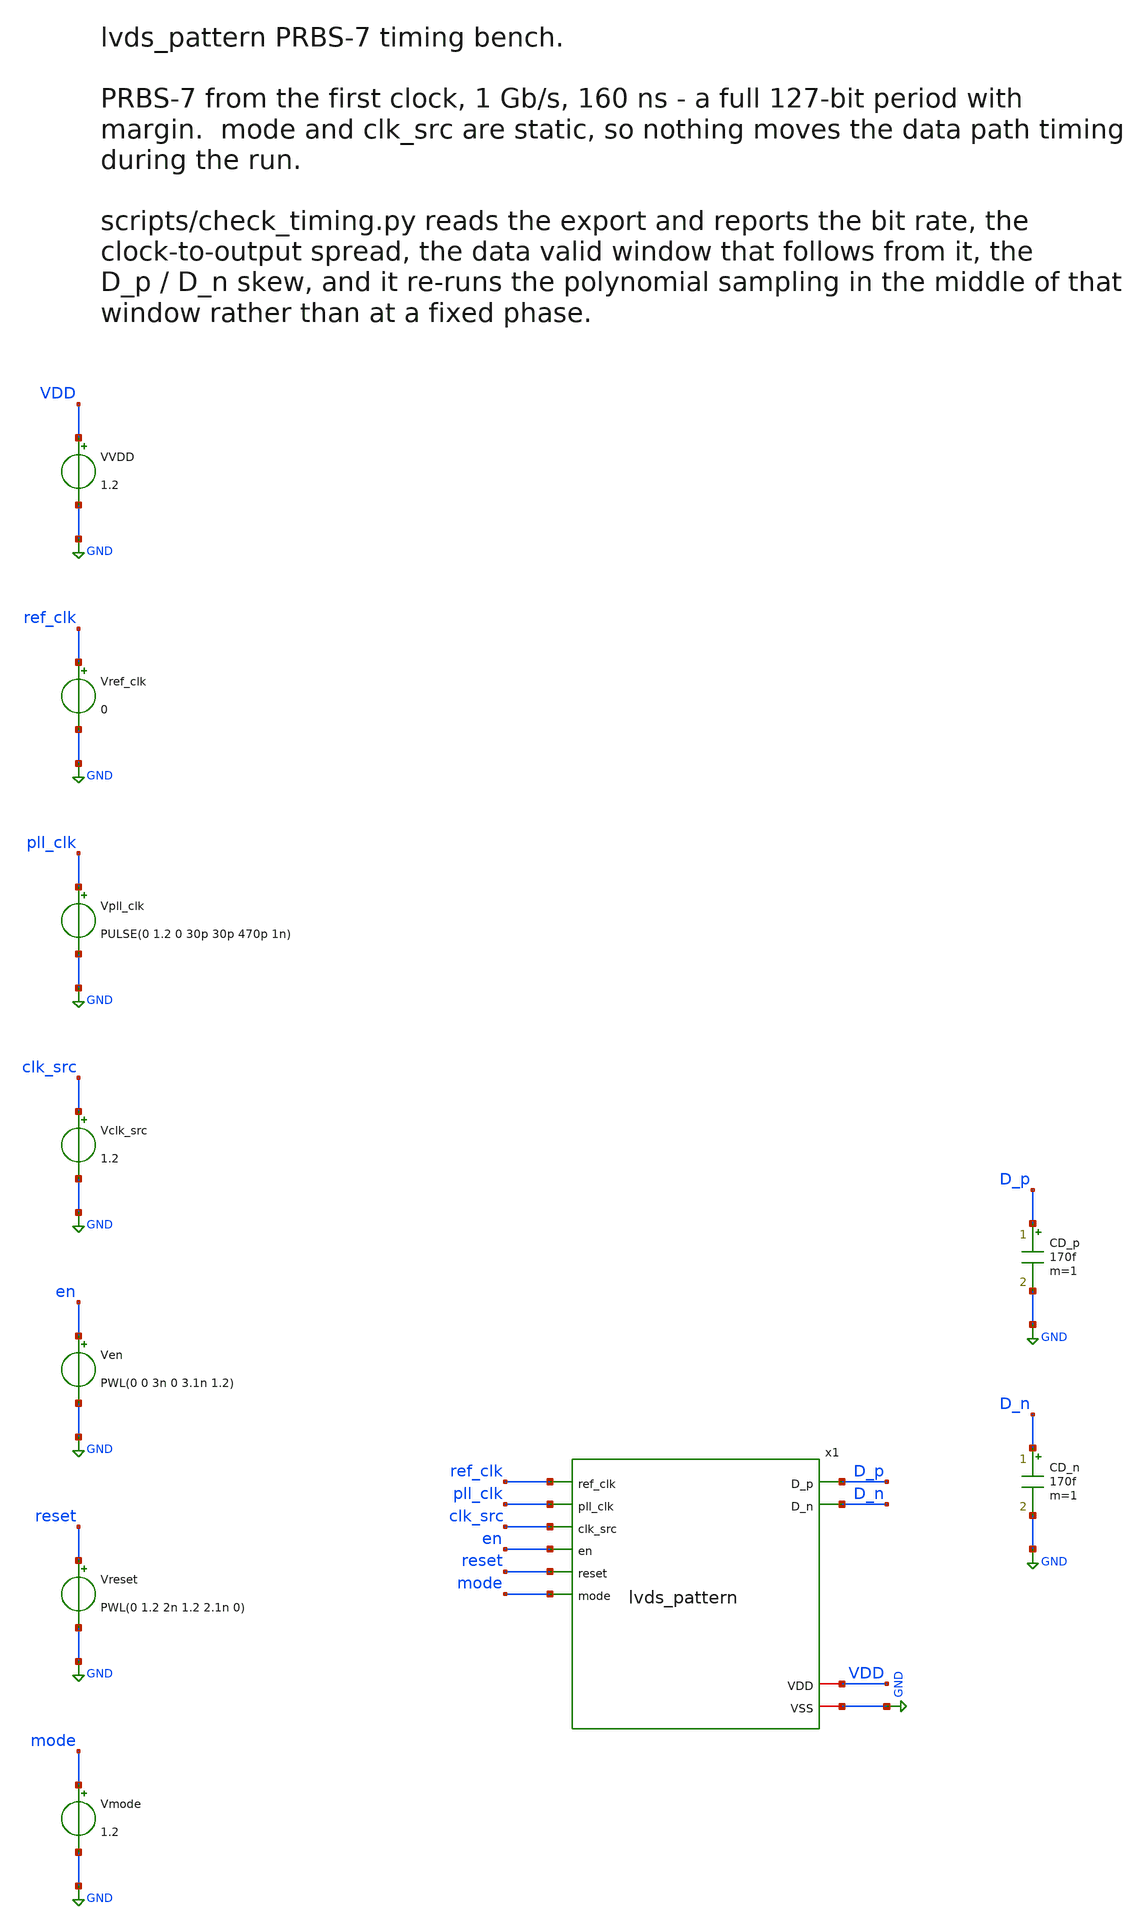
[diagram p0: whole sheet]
** sch_path: macros/lvds_pattern/testbenches/xschem/lvds_pattern_tb_prbs.sch
**.subckt lvds_pattern_tb_prbs
VVDD VDD GND 1.2
Vref_clk ref_clk GND 0
Vpll_clk pll_clk GND PULSE(0 1.2 0 30p 30p 470p 1n)
Vclk_src clk_src GND 1.2
Ven en GND PWL(0 0 3n 0 3.1n 1.2)
Vreset reset GND PWL(0 1.2 2n 1.2 2.1n 0)
Vmode mode GND 1.2
x1 ref_clk pll_clk clk_src en reset mode D_p D_n VDD GND lvds_pattern
CD_p D_p GND 170f m=1
CD_n D_n GND 170f m=1
**** begin user architecture code


.include /foss/pdks/ihp-sg13cmos5l/libs.ref/sg13cmos5l_stdcell/spice/sg13cmos5l_stdcell.spice
.lib cornerMOSlv.lib mos_tt
.temp 27
.options savecurrents klu reltol=1e-3
.control
save D_p D_n x1.gclk_b x1.s6 x1.s6_n x1.fp x1.fn mode en reset
tran 2p 160n
write @schname\.raw

* the pair has to be complementary at every instant
let dsum = v(D_p)+v(D_n)
meas tran dsum_min MIN dsum from=10n to=155n
meas tran dsum_max MAX dsum from=10n to=155n
print dsum_min dsum_max

set wr_vecnames
set wr_singlescale
wrdata ../plot_simulations/data/@schname\.txt  v(D_p) v(D_n) v(x1.gclk_b)
.endc


**** end user architecture code
**.ends

* expanding   symbol:  lvds_pattern.sym # of pins=10
** sym_path: macros/lvds_pattern/schematic/xschem/lvds_pattern.sym
** sch_path: macros/lvds_pattern/schematic/xschem/lvds_pattern.sch
.subckt lvds_pattern ref_clk pll_clk clk_src en reset mode D_p D_n VDD VSS
*.ipin ref_clk
*.ipin pll_clk
*.ipin clk_src
*.ipin en
*.ipin reset
*.ipin mode
*.opin D_p
*.opin D_n
*.iopin VDD
*.iopin VSS
xcsel clk_sel ref_clk pll_clk clk_src VDD VSS sg13cmos5l_mux2_2
xicg gclk clk_sel en VDD VSS sg13cmos5l_lgcp_1
xclkb gclk_b gclk VDD VSS sg13cmos5l_buf_4
xrstb reset_b reset VDD VSS sg13cmos5l_inv_2
xs0 s0 s0_n gclk_b fb reset_b VDD VSS sg13cmos5l_dfrbp_1
xs1 s1 s1_n gclk_b s0 reset_b VDD VSS sg13cmos5l_dfrbp_1
xs2 s2 s2_n gclk_b s1 reset_b VDD VSS sg13cmos5l_dfrbp_1
xs3 s3 s3_n gclk_b s2 reset_b VDD VSS sg13cmos5l_dfrbp_1
xs4 s4 s4_n gclk_b s3 reset_b VDD VSS sg13cmos5l_dfrbp_1
xs5 s5 s5_n gclk_b s4 reset_b VDD VSS sg13cmos5l_dfrbp_2
xs6 s6 s6_n gclk_b s5 reset_b VDD VSS sg13cmos5l_dfrbp_2
xfb fb s6 s5 VDD VSS sg13cmos5l_xnor2_1
xffp fp fp_n gclk_b s6 reset_b VDD VSS sg13cmos5l_dfrbp_2
xffn fn fn_n gclk_b s6_n reset_b VDD VSS sg13cmos5l_dfrbp_2
xclkn gclk_bn gclk_b VDD VSS sg13cmos5l_inv_2
xmodep dp0 gclk_bn fp mode VDD VSS sg13cmos5l_mux2_2
xmoden dn0 gclk_b fn mode VDD VSS sg13cmos5l_mux2_2
xp1 dp1 dp0 VDD VSS sg13cmos5l_inv_2
xp2 dp2 dp1 VDD VSS sg13cmos5l_inv_8
xbp D_p dp2 VDD VSS sg13cmos5l_inv_16
xn1 dn1 dn0 VDD VSS sg13cmos5l_inv_2
xn2 dn2 dn1 VDD VSS sg13cmos5l_inv_8
xbn D_n dn2 VDD VSS sg13cmos5l_inv_16
.ends

.GLOBAL GND
.end
